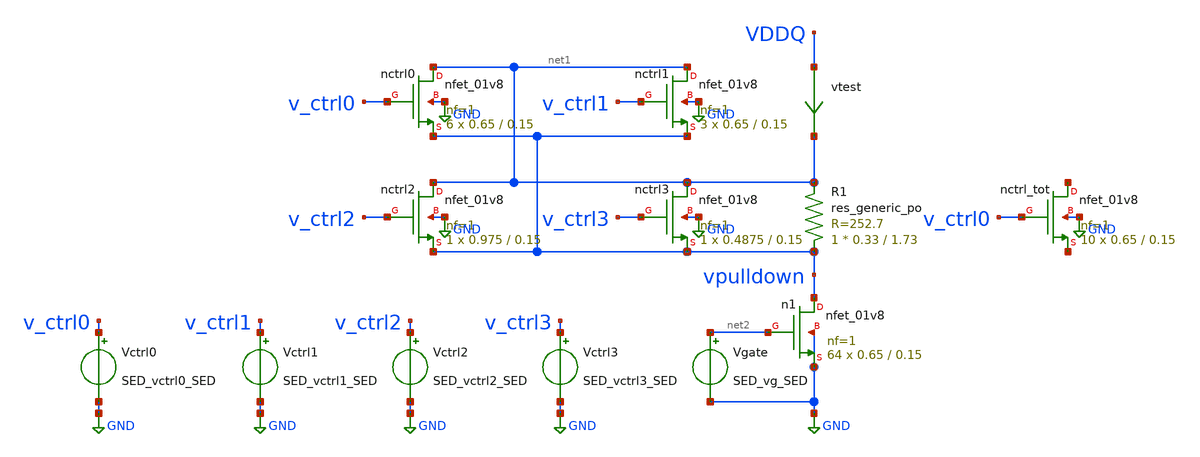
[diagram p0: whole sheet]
** sch_path: n-leg.sch
* Copyright 2021 Stefan Frederik Schippers
* Licensed under the Apache License, Version 2.0 (the "License");
* you may not use this file except in compliance with the License.
* You may obtain a copy of the License at
* https://www.apache.org/licenses/LICENSE-2.0
* Unless required by applicable law or agreed to in writing, software
* distributed under the License is distributed on an "AS IS" BASIS,
* WITHOUT WARRANTIES OR CONDITIONS OF ANY KIND, either express or implied.
* See the License for the specific language governing permissions and
* limitations under the License.
**.subckt n-leg
XR1 vpulldown net1 sky130_fd_pr__res_generic_po W=0.33 L=1.73 m=1
vtest VDDQ net1 0
.save i(vtest)
Xn1 vpulldown net2 GND GND sky130_fd_pr__nfet_01v8 L=0.15 W=0.65 nf=1 ad='int((nf+1)/2) * W/nf * 0.29'
+ as='int((nf+2)/2) * W/nf * 0.29' pd='2*int((nf+1)/2) * (W/nf + 0.29)' ps='2*int((nf+2)/2) * (W/nf + 0.29)'
+ nrd='0.29 / W' nrs='0.29 / W' sa=0 sb=0 sd=0 mult=64 m=64
Vgate net2 GND SED_vg_SED
Xnctrl0 net1 v_ctrl0 vpulldown GND sky130_fd_pr__nfet_01v8 L=0.15 W=0.65 nf=1 ad='int((nf+1)/2) * W/nf * 0.29'
+ as='int((nf+2)/2) * W/nf * 0.29' pd='2*int((nf+1)/2) * (W/nf + 0.29)' ps='2*int((nf+2)/2) * (W/nf + 0.29)'
+ nrd='0.29 / W' nrs='0.29 / W' sa=0 sb=0 sd=0 mult=6 m=6
Vctrl0 v_ctrl0 GND SED_vctrl0_SED
Xnctrl1 net1 v_ctrl1 vpulldown GND sky130_fd_pr__nfet_01v8 L=0.15 W=0.65 nf=1 ad='int((nf+1)/2) * W/nf * 0.29'
+ as='int((nf+2)/2) * W/nf * 0.29' pd='2*int((nf+1)/2) * (W/nf + 0.29)' ps='2*int((nf+2)/2) * (W/nf + 0.29)'
+ nrd='0.29 / W' nrs='0.29 / W' sa=0 sb=0 sd=0 mult=3 m=3
Xnctrl2 net1 v_ctrl2 vpulldown GND sky130_fd_pr__nfet_01v8 L=0.15 W=0.975 nf=1 ad='int((nf+1)/2) * W/nf * 0.29'
+ as='int((nf+2)/2) * W/nf * 0.29' pd='2*int((nf+1)/2) * (W/nf + 0.29)' ps='2*int((nf+2)/2) * (W/nf + 0.29)'
+ nrd='0.29 / W' nrs='0.29 / W' sa=0 sb=0 sd=0 mult=1 m=1
Xnctrl3 net1 v_ctrl3 vpulldown GND sky130_fd_pr__nfet_01v8 L=0.15 W=0.4875 nf=1 ad='int((nf+1)/2) * W/nf * 0.29'
+ as='int((nf+2)/2) * W/nf * 0.29' pd='2*int((nf+1)/2) * (W/nf + 0.29)' ps='2*int((nf+2)/2) * (W/nf + 0.29)'
+ nrd='0.29 / W' nrs='0.29 / W' sa=0 sb=0 sd=0 mult=1 m=1
Xnctrl_tot net3 v_ctrl0 net4 GND sky130_fd_pr__nfet_01v8 L=0.15 W=0.65 nf=1 ad='int((nf+1)/2) * W/nf * 0.29'
+ as='int((nf+2)/2) * W/nf * 0.29' pd='2*int((nf+1)/2) * (W/nf + 0.29)' ps='2*int((nf+2)/2) * (W/nf + 0.29)'
+ nrd='0.29 / W' nrs='0.29 / W' sa=0 sb=0 sd=0 mult=10 m=10
Vctrl1 v_ctrl1 GND SED_vctrl1_SED
Vctrl2 v_ctrl2 GND SED_vctrl2_SED
Vctrl3 v_ctrl3 GND SED_vctrl3_SED
**** begin user architecture code
 ** Local library links to pdk
.lib ./libs/SED_process_SED_lib.spice SED_process_SED

**** end user architecture code
**.ends
.GLOBAL GND
**** begin user architecture code



* power voltage
vvddq VDDQ 0 0
*.param rwidth=4.6

.control
save all
set temp=SED_temp_SED

* RUN SIMULATION
dc vvddq 0.3 1.2 0.05
* OUTPUT
print v(vddq)/i(vtest)
wrdata out/data/SED_plotName_SED.txt v(vddq)/i(vtest)
set hcopydevtype = svg
hardcopy ./out/plots/SED_plotName_SED.svg vddq/I(vtest) vs vddq title 'Resistance vs pin voltage'

.endc


**** end user architecture code
.end
